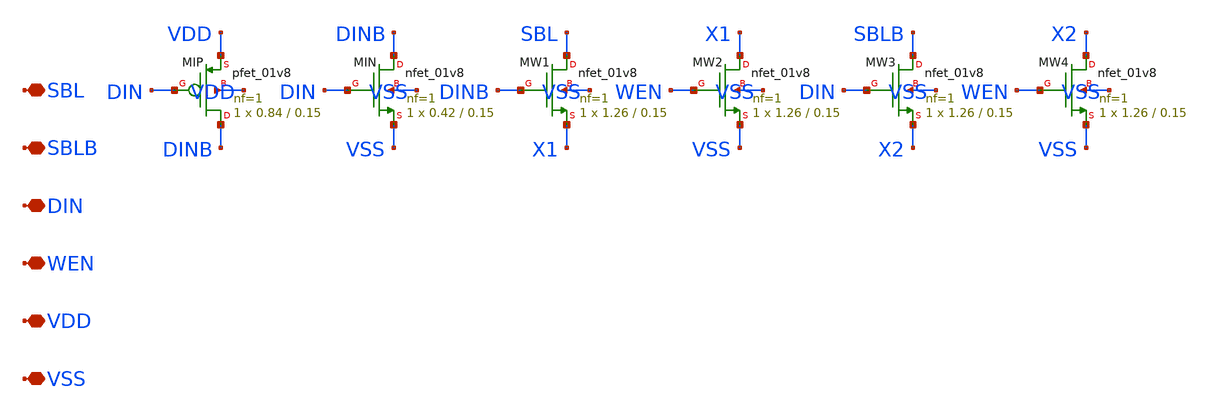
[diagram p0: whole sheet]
** sch_path: design/compiler/cells/sram_wdrv.sch
**.subckt sram_wdrv SBL SBLB DIN WEN VDD VSS
*.iopin SBL
*.iopin SBLB
*.iopin DIN
*.iopin WEN
*.iopin VDD
*.iopin VSS
XMIP DINB DIN VDD VDD sky130_fd_pr__pfet_01v8 L=0.15 W=0.84 nf=1 ad=0.2436 as=0.2436 pd=2.26 ps=2.26
+ nrd=0.3452 nrs=0.3452 sa=0 sb=0 sd=0 mult=1 m=1
XMIN DINB DIN VSS VSS sky130_fd_pr__nfet_01v8 L=0.15 W=0.42 nf=1 ad=0.1218 as=0.1218 pd=1.42 ps=1.42
+ nrd=0.6905 nrs=0.6905 sa=0 sb=0 sd=0 mult=1 m=1
XMW1 SBL DINB X1 VSS sky130_fd_pr__nfet_01v8 L=0.15 W=1.26 nf=1 ad=0.3654 as=0.3654 pd=3.1 ps=3.1
+ nrd=0.2302 nrs=0.2302 sa=0 sb=0 sd=0 mult=1 m=1
XMW2 X1 WEN VSS VSS sky130_fd_pr__nfet_01v8 L=0.15 W=1.26 nf=1 ad=0.3654 as=0.3654 pd=3.1 ps=3.1
+ nrd=0.2302 nrs=0.2302 sa=0 sb=0 sd=0 mult=1 m=1
XMW3 SBLB DIN X2 VSS sky130_fd_pr__nfet_01v8 L=0.15 W=1.26 nf=1 ad=0.3654 as=0.3654 pd=3.1 ps=3.1
+ nrd=0.2302 nrs=0.2302 sa=0 sb=0 sd=0 mult=1 m=1
XMW4 X2 WEN VSS VSS sky130_fd_pr__nfet_01v8 L=0.15 W=1.26 nf=1 ad=0.3654 as=0.3654 pd=3.1 ps=3.1
+ nrd=0.2302 nrs=0.2302 sa=0 sb=0 sd=0 mult=1 m=1
**.ends
.end
